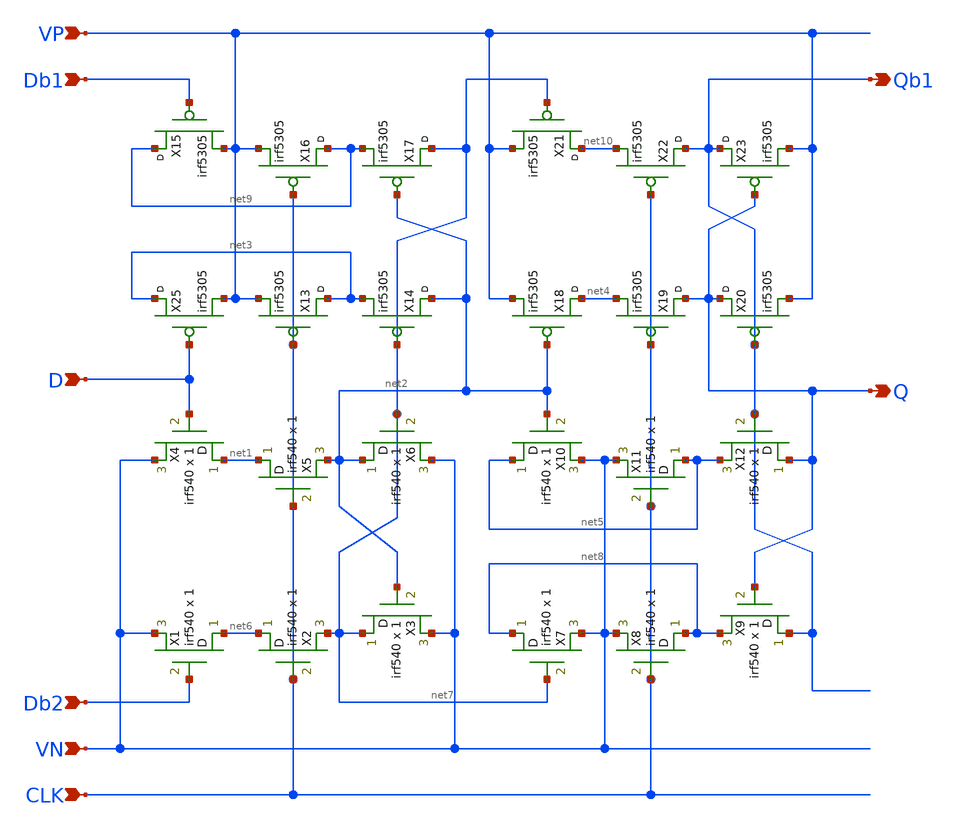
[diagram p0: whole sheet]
** sch_path: projects/negdff/xschem_ngspice/negdff.sch
**.subckt negdff D Db1 Db2 Q Qb1 CLK VP VN
*.ipin D
*.ipin Db1
*.ipin Db2
*.opin Q
*.opin Qb1
*.ipin CLK
*.ipin VP
*.ipin VN
X1 net6 Db2 VN irf540 m=1
X2 net6 CLK net7 irf540 m=1
X3 net7 net2 VN irf540 m=1
X4 net1 D VN irf540 m=1
X5 net1 CLK net2 irf540 m=1
X6 net2 net7 VN irf540 m=1
X7 net8 net7 VN irf540 m=1
X8 net8 CLK VN irf540 m=1
X9 Qb1 Q net8 irf540 m=1
X10 net5 net2 VN irf540 m=1
X11 net5 CLK VN irf540 m=1
X12 Q Qb1 net5 irf540 m=1
X25 net3 D VP irf5305
X13 net3 CLK VP irf5305
X14 net2 net7 net3 irf5305
X15 net9 Db1 VP irf5305
X16 net9 CLK VP irf5305
X17 net7 net2 net9 irf5305
X18 net4 net2 VP irf5305
X19 Q CLK net4 irf5305
X20 Q Qb1 VP irf5305
X21 net10 net7 VP irf5305
X22 Qb1 CLK net10 irf5305
X23 Qb1 Q VP irf5305
**.ends
.end
